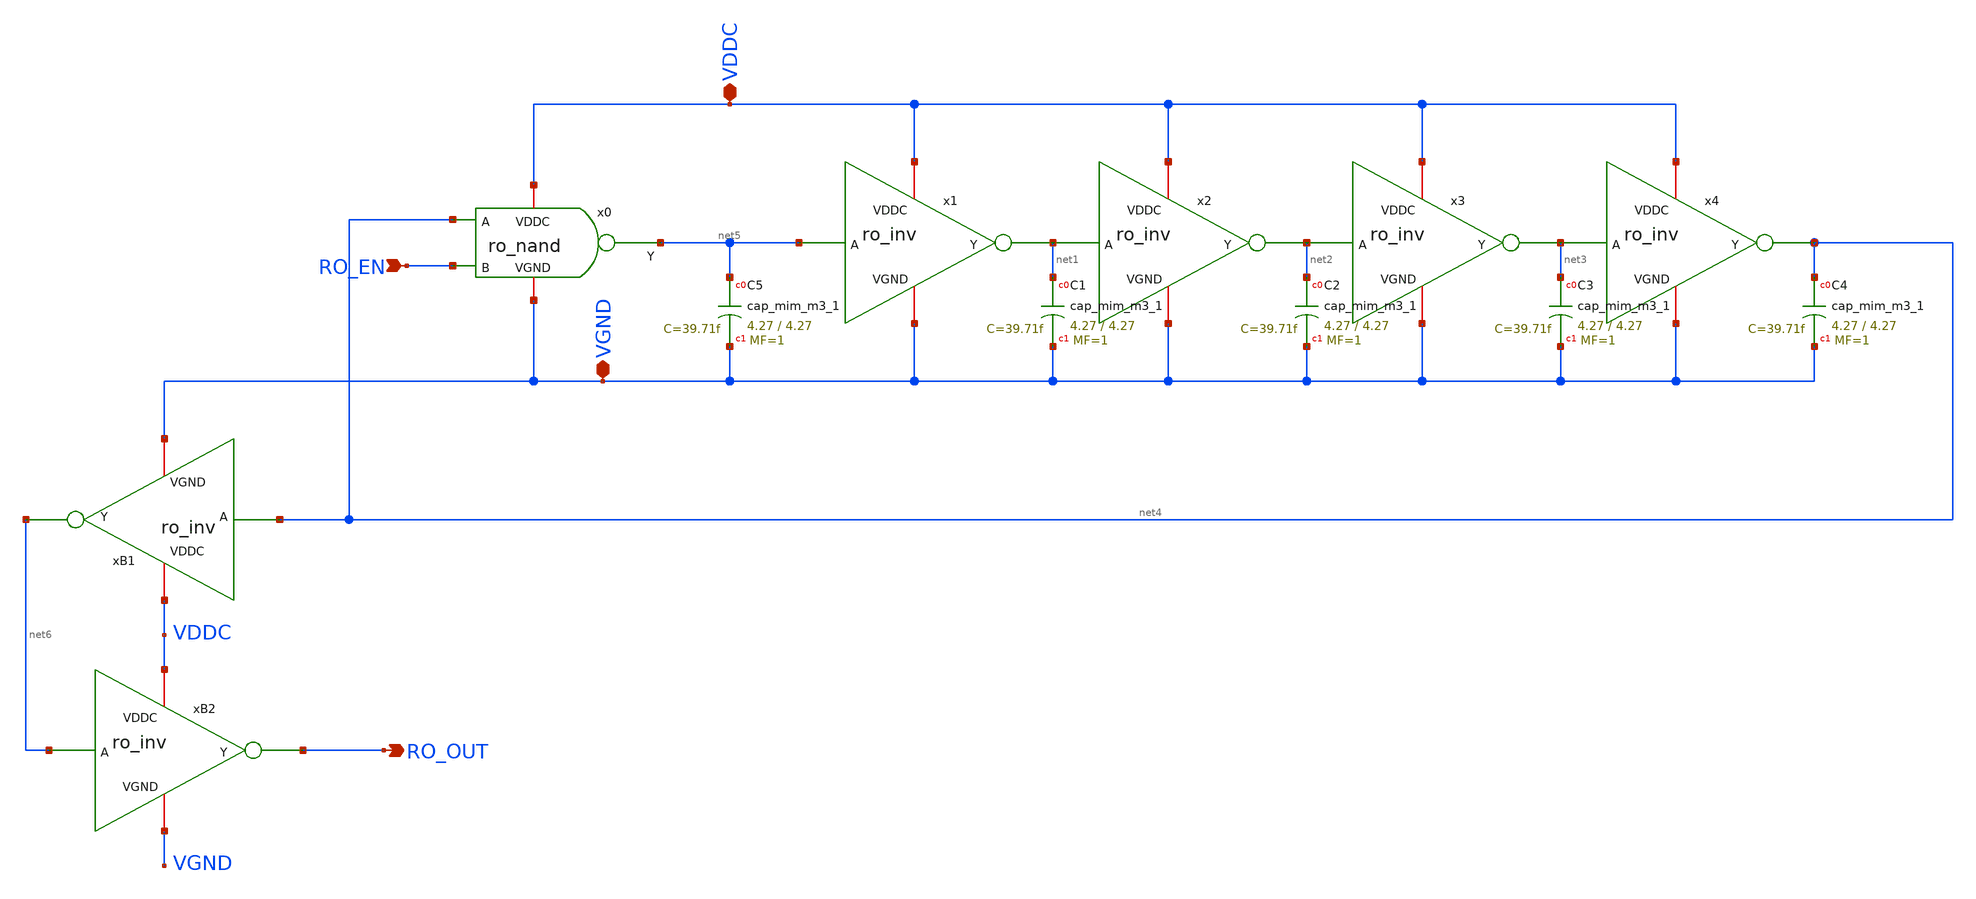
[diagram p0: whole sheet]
** sch_path: designs/bgr_ldo/ldo/ring_osc_core.sch
**.subckt ring_osc_core VDDC VGND RO_OUT RO_EN
*.iopin VDDC
*.iopin VGND
*.opin RO_OUT
*.ipin RO_EN
x1 VDDC net5 net1 VGND ro_inv
x0 VDDC net4 RO_EN net5 VGND ro_nand
XC1 net1 VGND sky130_fd_pr__cap_mim_m3_1 W=4.27 L=4.27 MF=1 m=1
x2 VDDC net1 net2 VGND ro_inv
XC2 net2 VGND sky130_fd_pr__cap_mim_m3_1 W=4.27 L=4.27 MF=1 m=1
x3 VDDC net2 net3 VGND ro_inv
XC3 net3 VGND sky130_fd_pr__cap_mim_m3_1 W=4.27 L=4.27 MF=1 m=1
XC4 net4 VGND sky130_fd_pr__cap_mim_m3_1 W=4.27 L=4.27 MF=1 m=1
xB1 VDDC net4 net6 VGND ro_inv
xB2 VDDC net6 RO_OUT VGND ro_inv
XC5 net5 VGND sky130_fd_pr__cap_mim_m3_1 W=4.27 L=4.27 MF=1 m=1
x4 VDDC net3 net4 VGND ro_inv
**.ends

* expanding   symbol:  ro_inv.sym # of pins=4
** sym_path: designs/bgr_ldo/ldo/ro_inv.sym
** sch_path: designs/bgr_ldo/ldo/ro_inv.sch
.subckt ro_inv VDDC A Y VGND
*.iopin VDDC
*.iopin VGND
*.ipin A
*.opin Y
XMP Y A VDDC VDDC sky130_fd_pr__pfet_01v8 L=0.15 W=1 nf=1 ad='int((1 + 1)/2) * 1 / 1 * 0.29' as='int((1 + 2)/2) * 1 / 1 * 0.29'
+ pd='2*int((1 + 1)/2) * (1 / 1 + 0.29)' ps='2*int((1 + 2)/2) * (1 / 1 + 0.29)' nrd='0.29 / 1 ' nrs='0.29 / 1 '
+ sa=0 sb=0 sd=0 mult=1 m=1
XMN Y A VGND VGND sky130_fd_pr__nfet_01v8 L=0.15 W=0.42 nf=1 ad='int((1 + 1)/2) * 0.42 / 1 * 0.29' as='int((1 + 2)/2) * 0.42 / 1 * 0.29'
+ pd='2*int((1 + 1)/2) * (0.42 / 1 + 0.29)' ps='2*int((1 + 2)/2) * (0.42 / 1 + 0.29)' nrd='0.29 / 0.42 '
+ nrs='0.29 / 0.42 ' sa=0 sb=0 sd=0 mult=1 m=1
.ends


* expanding   symbol:  ro_nand.sym # of pins=5
** sym_path: designs/bgr_ldo/ldo/ro_nand.sym
** sch_path: designs/bgr_ldo/ldo/ro_nand.sch
.subckt ro_nand VDDC A B Y VGND
*.iopin VDDC
*.iopin VGND
*.ipin A
*.opin Y
*.ipin B
XMP1 Y B VDDC VDDC sky130_fd_pr__pfet_01v8 L=0.15 W=1 nf=1 ad='int((1 + 1)/2) * 1 / 1 * 0.29' as='int((1 + 2)/2) * 1 / 1 * 0.29'
+ pd='2*int((1 + 1)/2) * (1 / 1 + 0.29)' ps='2*int((1 + 2)/2) * (1 / 1 + 0.29)' nrd='0.29 / 1 ' nrs='0.29 / 1 '
+ sa=0 sb=0 sd=0 mult=1 m=1
XMP2 Y A VDDC VDDC sky130_fd_pr__pfet_01v8 L=0.15 W=1 nf=1 ad='int((1 + 1)/2) * 1 / 1 * 0.29' as='int((1 + 2)/2) * 1 / 1 * 0.29'
+ pd='2*int((1 + 1)/2) * (1 / 1 + 0.29)' ps='2*int((1 + 2)/2) * (1 / 1 + 0.29)' nrd='0.29 / 1 ' nrs='0.29 / 1 '
+ sa=0 sb=0 sd=0 mult=1 m=1
XMN1 Y A n_nandmid VGND sky130_fd_pr__nfet_01v8 L=0.15 W=1 nf=1 ad='int((1 + 1)/2) * 1 / 1 * 0.29' as='int((1 + 2)/2) * 1 / 1 * 0.29'
+ pd='2*int((1 + 1)/2) * (1 / 1 + 0.29)' ps='2*int((1 + 2)/2) * (1 / 1 + 0.29)' nrd='0.29 / 1 ' nrs='0.29 / 1 '
+ sa=0 sb=0 sd=0 mult=1 m=1
XMN2 n_nandmid B VGND VGND sky130_fd_pr__nfet_01v8 L=0.15 W=1 nf=1 ad='int((1 + 1)/2) * 1 / 1 * 0.29'
+ as='int((1 + 2)/2) * 1 / 1 * 0.29' pd='2*int((1 + 1)/2) * (1 / 1 + 0.29)' ps='2*int((1 + 2)/2) * (1 / 1 + 0.29)'
+ nrd='0.29 / 1 ' nrs='0.29 / 1 ' sa=0 sb=0 sd=0 mult=1 m=1
.ends

.end
